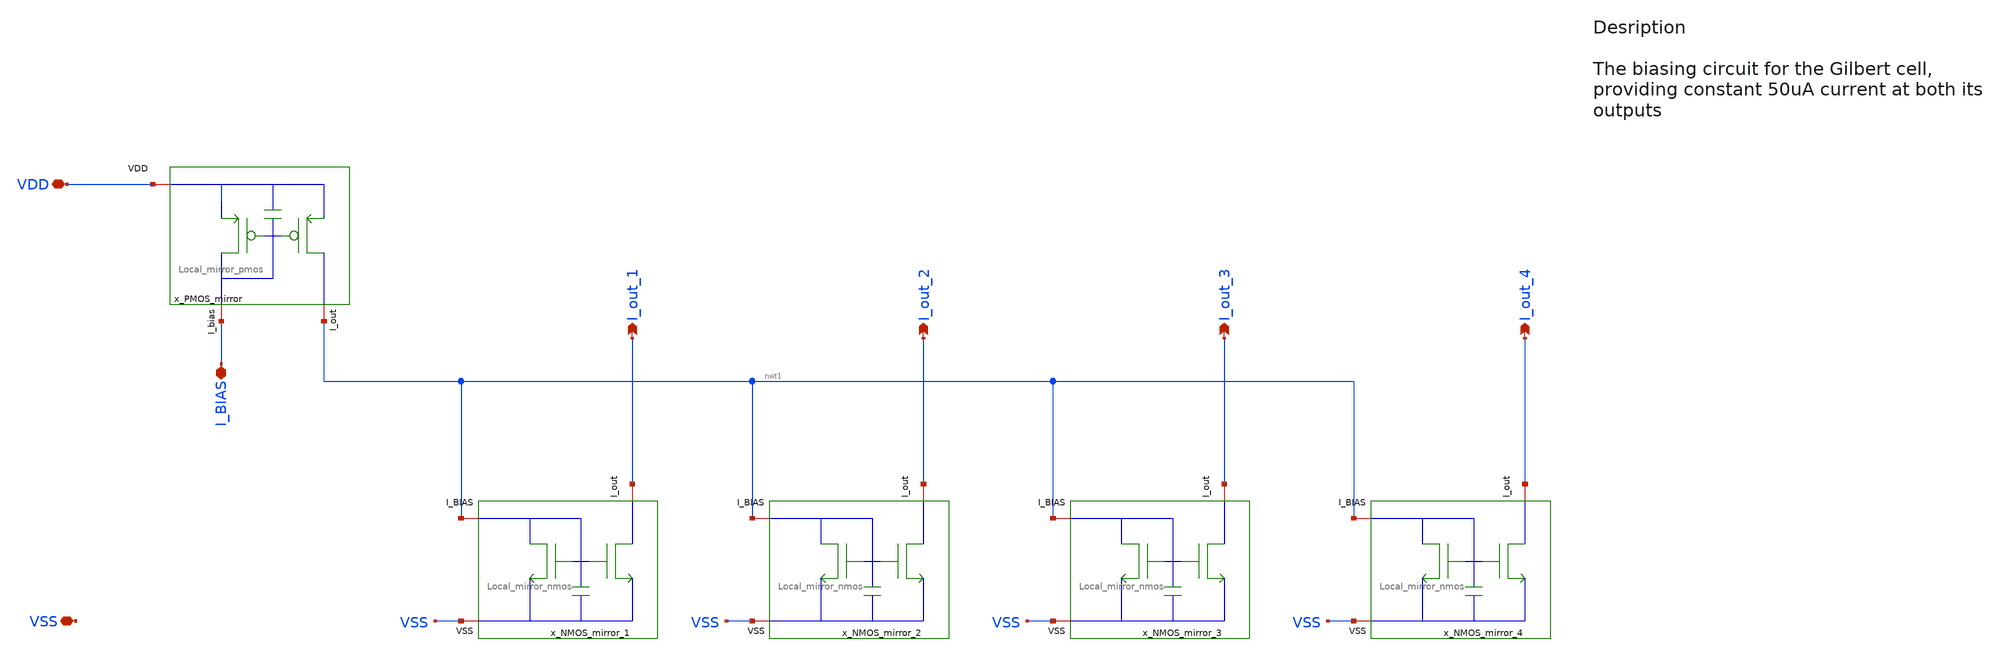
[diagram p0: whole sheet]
** sch_path: src/design_xsch/Biasing_network_with_local_mirros.sch
**.subckt Biasing_network_with_local_mirros VSS I_BIAS I_out_1 I_out_2 I_out_3 VDD I_out_4
*.iopin VSS
*.iopin I_BIAS
*.opin I_out_1
*.opin I_out_2
*.opin I_out_3
*.iopin VDD
*.opin I_out_4
x_PMOS_mirror VDD net1 I_BIAS Local_mirror_pmos w_ref=2u l_ref=0.4u w_mir=8u l_mir=0.4u
x_NMOS_mirror_1 I_out_1 net1 VSS Local_mirror_nmos l_ref=1u w_ref=1.5u nf_ref=1 l_mir=1u w_mir=7.5u
+ nf_mir=5
x_NMOS_mirror_2 I_out_2 net1 VSS Local_mirror_nmos l_ref=1u w_ref=1.5u nf_ref=1 l_mir=1u w_mir=7.5u
+ nf_mir=5
x_NMOS_mirror_3 I_out_3 net1 VSS Local_mirror_nmos l_ref=1u w_ref=1.5u nf_ref=1 l_mir=1u w_mir=6u
+ nf_mir=4
x_NMOS_mirror_4 I_out_4 net1 VSS Local_mirror_nmos l_ref=1u w_ref=1.5u nf_ref=1 l_mir=1u w_mir=15u
+ nf_mir=10
**** begin user architecture code

.include $::180MCU_MODELS/design.ngspice
.lib $::180MCU_MODELS/sm141064.ngspice typical
.lib $::180MCU_MODELS/sm141064.ngspice mimcap_typical
.lib $::180MCU_MODELS/sm141064.ngspice cap_mim
.lib $::180MCU_MODELS/sm141064.ngspice res_typical




* let sets vectors to a plot, while set sets a variable, globally accessible in .control
.control

    * Set frequency and amplitude variables to proper values from within the control sequence
    save all

    op
    show

    write Biasing_network_sim.raw

    set appendwrite

    * Transient analysis to observe mixing operation
    tran 1p 10n


    write Biasing_network_sim.raw

.endc


**** end user architecture code
**.ends
.end
